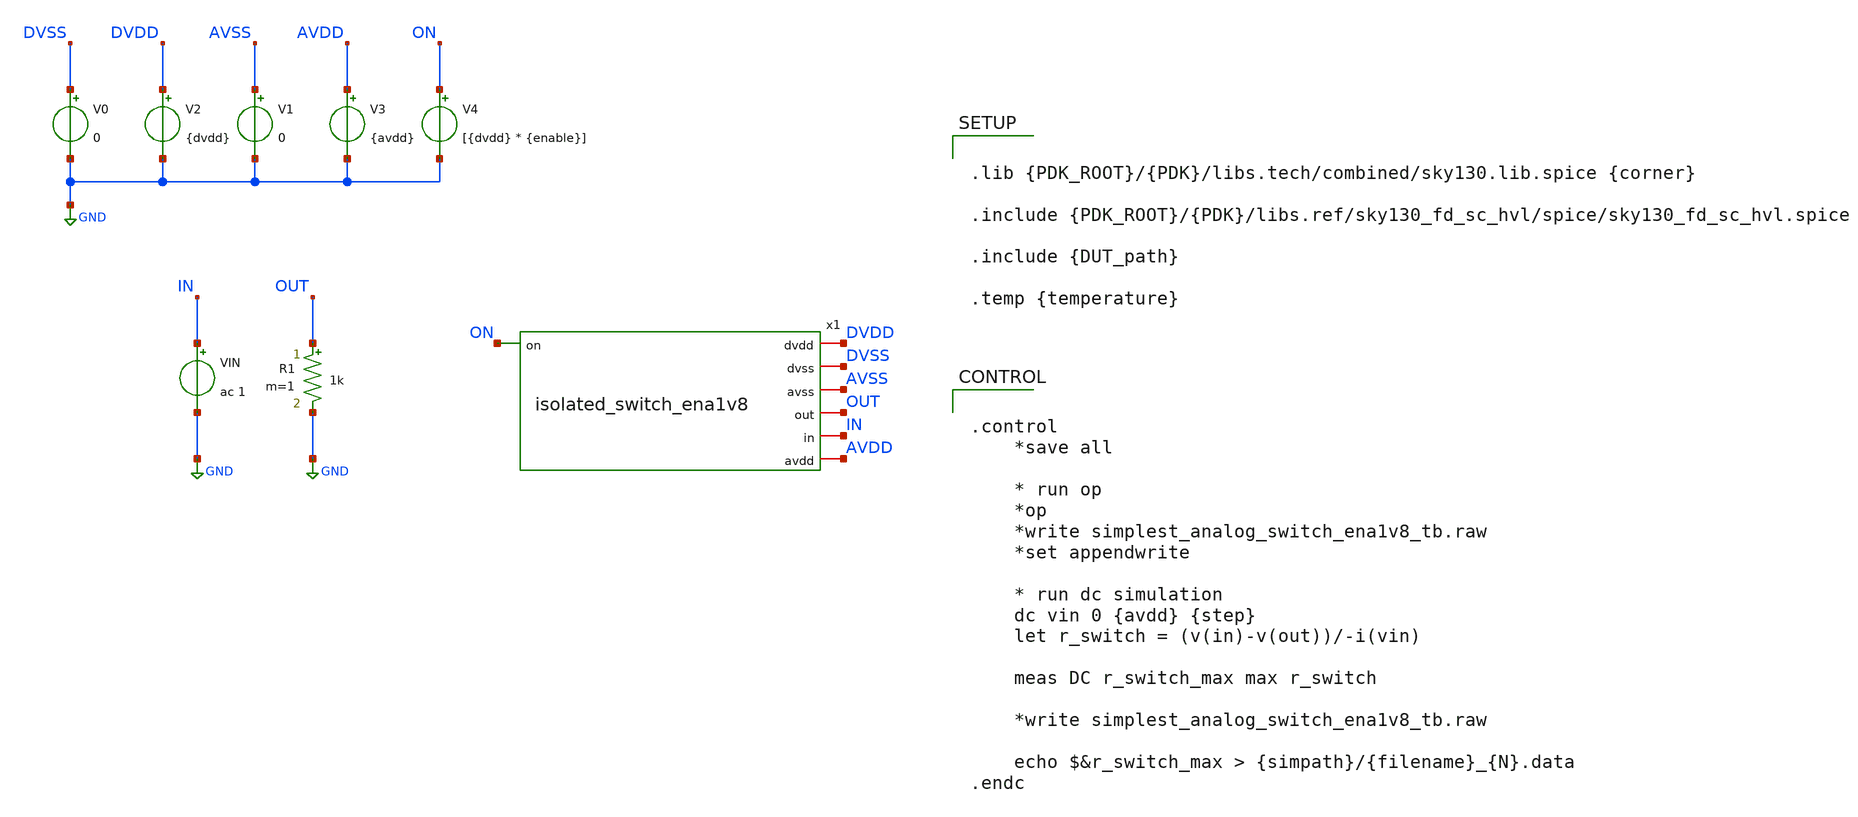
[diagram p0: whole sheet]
** sch_path: cace/templates/isolated_switch_ena1v8_tb.sch
**.subckt isolated_switch_ena1v8_tb
V0 DVSS GND 0
V2 DVDD GND {dvdd}
V1 AVSS GND 0
V3 AVDD GND {avdd}
V4 ON GND [{dvdd} * {enable}]
VIN IN GND ac 1
R1 OUT GND 1k m=1
x1 AVSS ON OUT IN AVDD DVDD DVSS isolated_switch_ena1v8
**** begin user architecture code


.lib {PDK_ROOT}/{PDK}/libs.tech/combined/sky130.lib.spice {corner}

.include {PDK_ROOT}/{PDK}/libs.ref/sky130_fd_sc_hvl/spice/sky130_fd_sc_hvl.spice

.include {DUT_path}

.temp {temperature}




.control
    *save all

    * run op
    *op
    *write simplest_analog_switch_ena1v8_tb.raw
    *set appendwrite

    * run dc simulation
    dc vin 0 {avdd} {step}
    let r_switch = (v(in)-v(out))/-i(vin)

    meas DC r_switch_max max r_switch

    *write simplest_analog_switch_ena1v8_tb.raw

    echo $&r_switch_max > {simpath}/{filename}_{N}.data
.endc


**** end user architecture code
**.ends
.GLOBAL GND
.end
